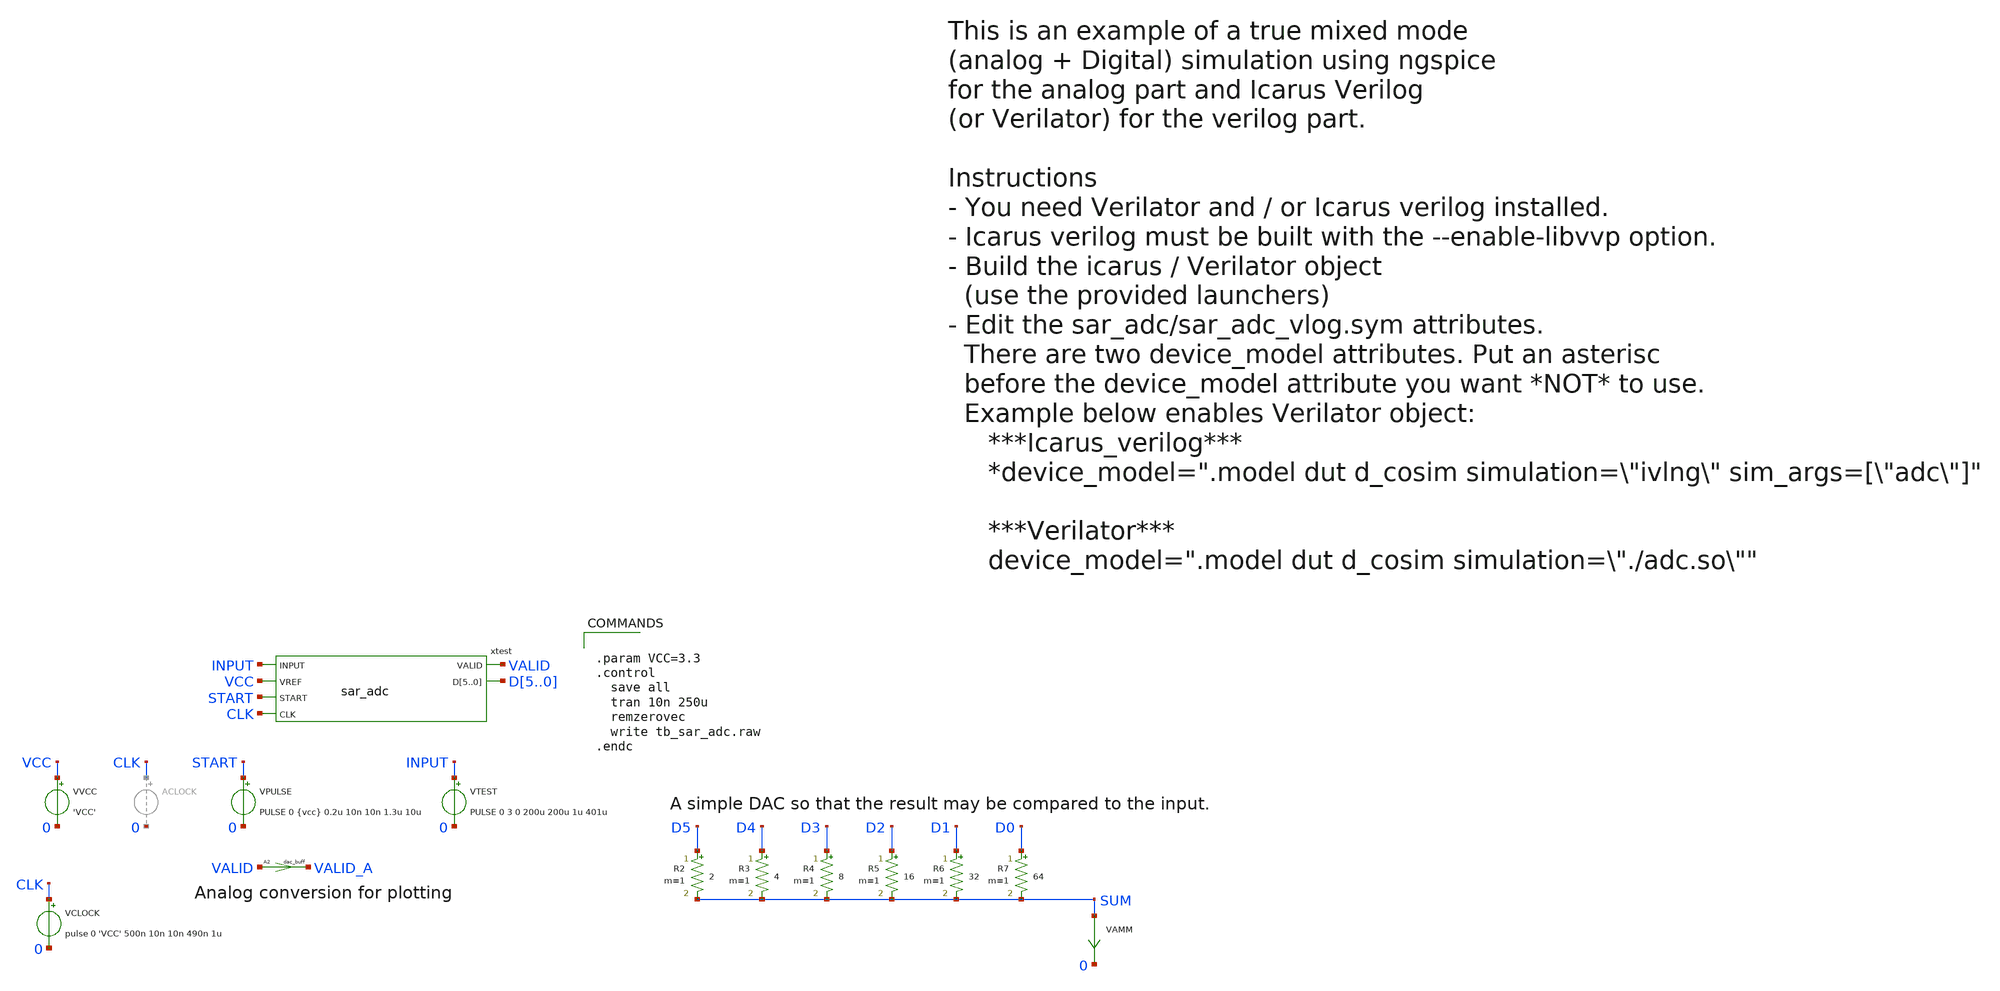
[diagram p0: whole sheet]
** sch_path: xschem_library/ngspice_verilog_cosim/tb_sar_adc.sch
**.subckt tb_sar_adc
VAMM SUM 0 0
VPULSE START 0 PULSE 0 {vcc} 0.2u 10n 10n 1.3u 10u
VTEST INPUT 0 PULSE 0 3 0 200u 200u 1u 401u
VVCC VCC 0 'VCC'
R2 D5 SUM 2 m=1
R3 D4 SUM 4 m=1
R4 D3 SUM 8 m=1
R5 D2 SUM 16 m=1
R6 D1 SUM 32 m=1
R7 D0 SUM 64 m=1
xtest INPUT VCC START VALID D5 D4 D3 D2 D1 D0 CLK sar_adc
A2 [ VALID ] [ VALID_A ] dac_buff
VCLOCK CLK 0 pulse 0 'VCC' 500n 10n 10n 490n 1u
**** begin user architecture code


.param VCC=3.3
.control
  save all
  tran 10n 250u
  remzerovec
  write tb_sar_adc.raw
.endc


**** end user architecture code
**.ends

* expanding   symbol:  sar_adc.sym # of pins=6
** sym_path: xschem_library/ngspice_verilog_cosim/sar_adc.sym
** sch_path: xschem_library/ngspice_verilog_cosim/sar_adc.sch
.subckt sar_adc INPUT VREF START VALID D5 D4 D3 D2 D1 D0 CLK
*.ipin INPUT
*.ipin VREF
*.ipin START
*.opin VALID
*.ipin CLK
*.opin D5,D4,D3,D2,D1,D0
CLAST TEST_V 0 '1p / 32' m=1
ACOMP [ %vd(TEST_V VREF) ] [ COMP ] comparator
XSAMPLE INPUT IIN SAMPLE VREF tgate
R1 IIN TEST_V 1k m=1
ADUT [ CLK COMP START ] [ SAMPLE VALID ~D5 ~D4 ~D3 ~D2 ~D1 ~D0 ] dut
A1 [ COMP ] [ COMP_A ] dac_buff
* noconn D[5..0]
* noconn COMP
* noconn %vd(TEST_V VREF)
xb6 TEST_V VREF D5 ccap C=1p,'1p/2','1p/4','1p/8','1p/16','1p/32'
xb5 TEST_V VREF D4 ccap C=1p,'1p/2','1p/4','1p/8','1p/16','1p/32'
xb4 TEST_V VREF D3 ccap C=1p,'1p/2','1p/4','1p/8','1p/16','1p/32'
xb3 TEST_V VREF D2 ccap C=1p,'1p/2','1p/4','1p/8','1p/16','1p/32'
xb2 TEST_V VREF D1 ccap C=1p,'1p/2','1p/4','1p/8','1p/16','1p/32'
xb1 TEST_V VREF D0 ccap C=1p,'1p/2','1p/4','1p/8','1p/16','1p/32'
.ends


* expanding   symbol:  tgate.sym # of pins=4
** sym_path: xschem_library/ngspice_verilog_cosim/tgate.sym
** sch_path: xschem_library/ngspice_verilog_cosim/tgate.sch
.subckt tgate A B CTL VDD
*.ipin CTL
*.iopin B
*.iopin A
*.ipin VDD
SWITCH A B CTL 0 TG
* noconn VDD
.ends


* expanding   symbol:  ccap.sym # of pins=3
** sym_path: xschem_library/ngspice_verilog_cosim/ccap.sym
** sch_path: xschem_library/ngspice_verilog_cosim/ccap.sch
.subckt ccap IN VCC CTL  C=1p
*.ipin IN
*.ipin VCC
*.ipin CTL
XINV CTL TAIL VCC ainv
CB IN TAIL c='C' m=1
.ends


* expanding   symbol:  ainv.sym # of pins=3
** sym_path: xschem_library/ngspice_verilog_cosim/ainv.sym
** sch_path: xschem_library/ngspice_verilog_cosim/ainv.sch
.subckt ainv IN OUT VDD
*.ipin IN
*.opin OUT
*.ipin VDD
MN OUT IN 0 0 N1
MP OUT IN VDD VDD P1
.ends

**** begin user architecture code
.model dut d_cosim simulation="ivlng" sim_args=["adc"]
.model comparator adc_bridge in_low=0 in_high=0
.model n1 nmos   level=2 vto=0.5 kp=24e-6 gamma=0.15 phi=0.65 lambda=0.015 xj=0.5e-6

.model p1 pmos   level=2 vto=-0.5 kp=8.5e-6 gamma=0.4 phi=0.65 lambda=0.05 xj=0.5e-6

.MODEL TG SW( VT=1.5 RON=2k )
.model dac_buff dac_bridge input_load=1e-15 t_rise=10n t_fall=10n  out_low=0 out_high=3.3
**** end user architecture code
.end
